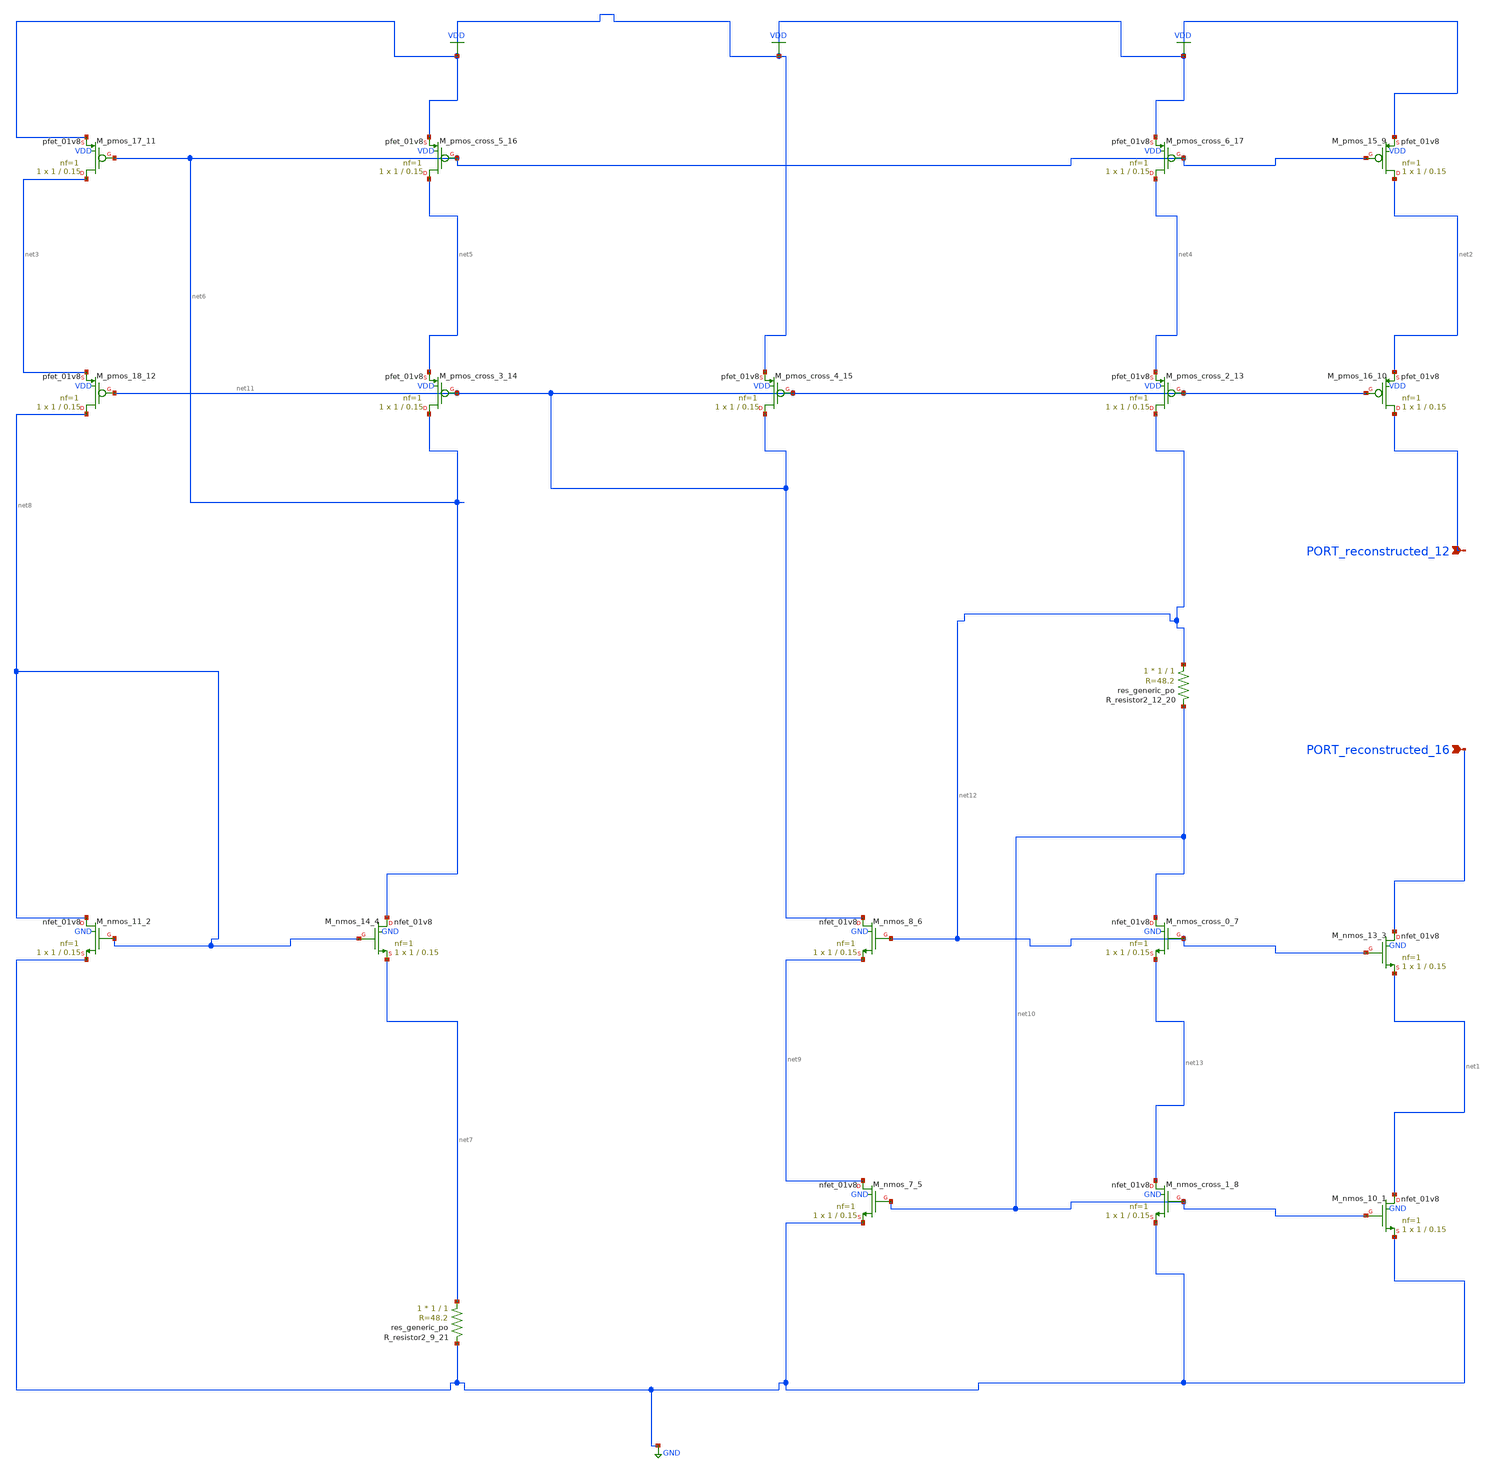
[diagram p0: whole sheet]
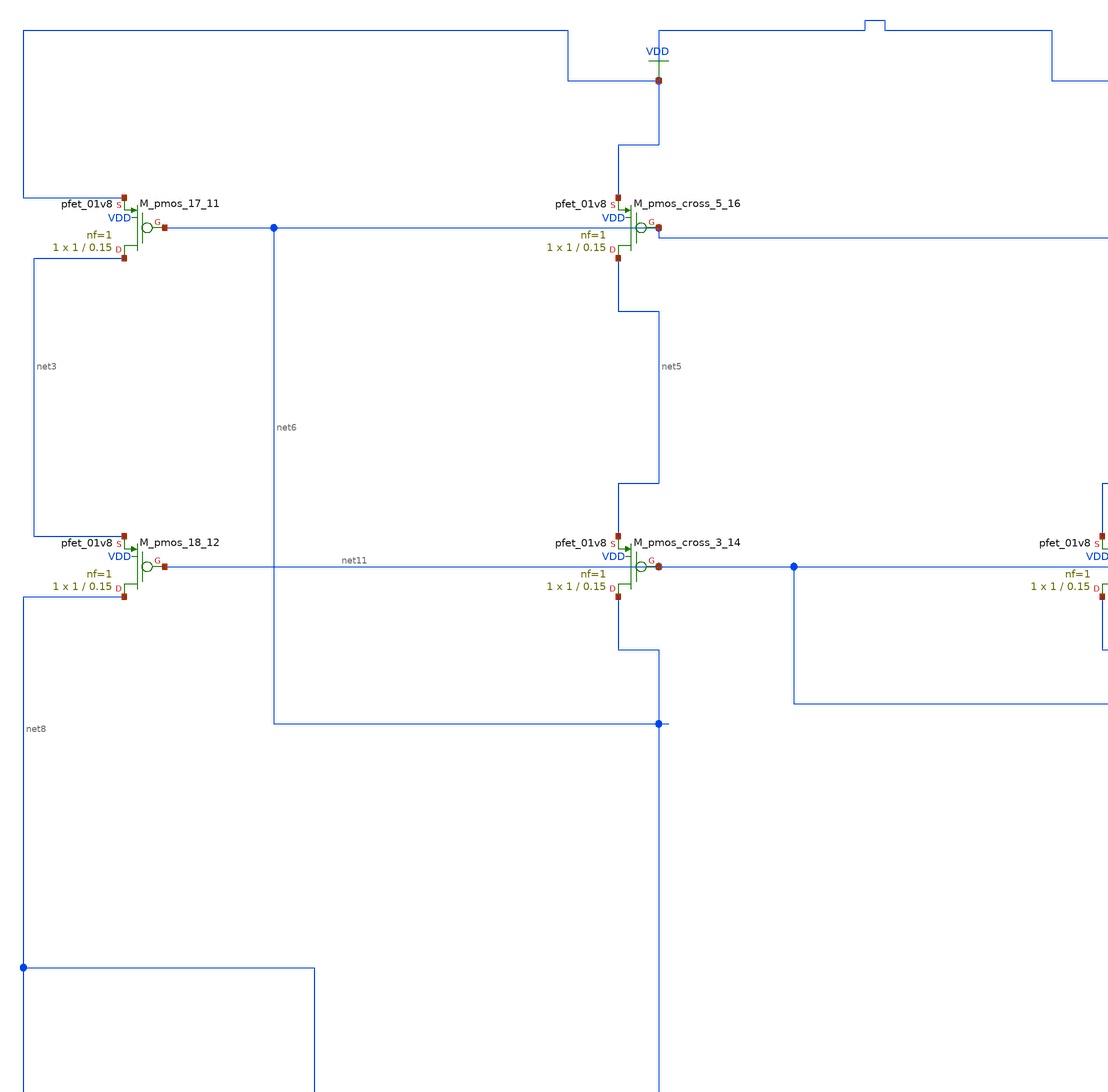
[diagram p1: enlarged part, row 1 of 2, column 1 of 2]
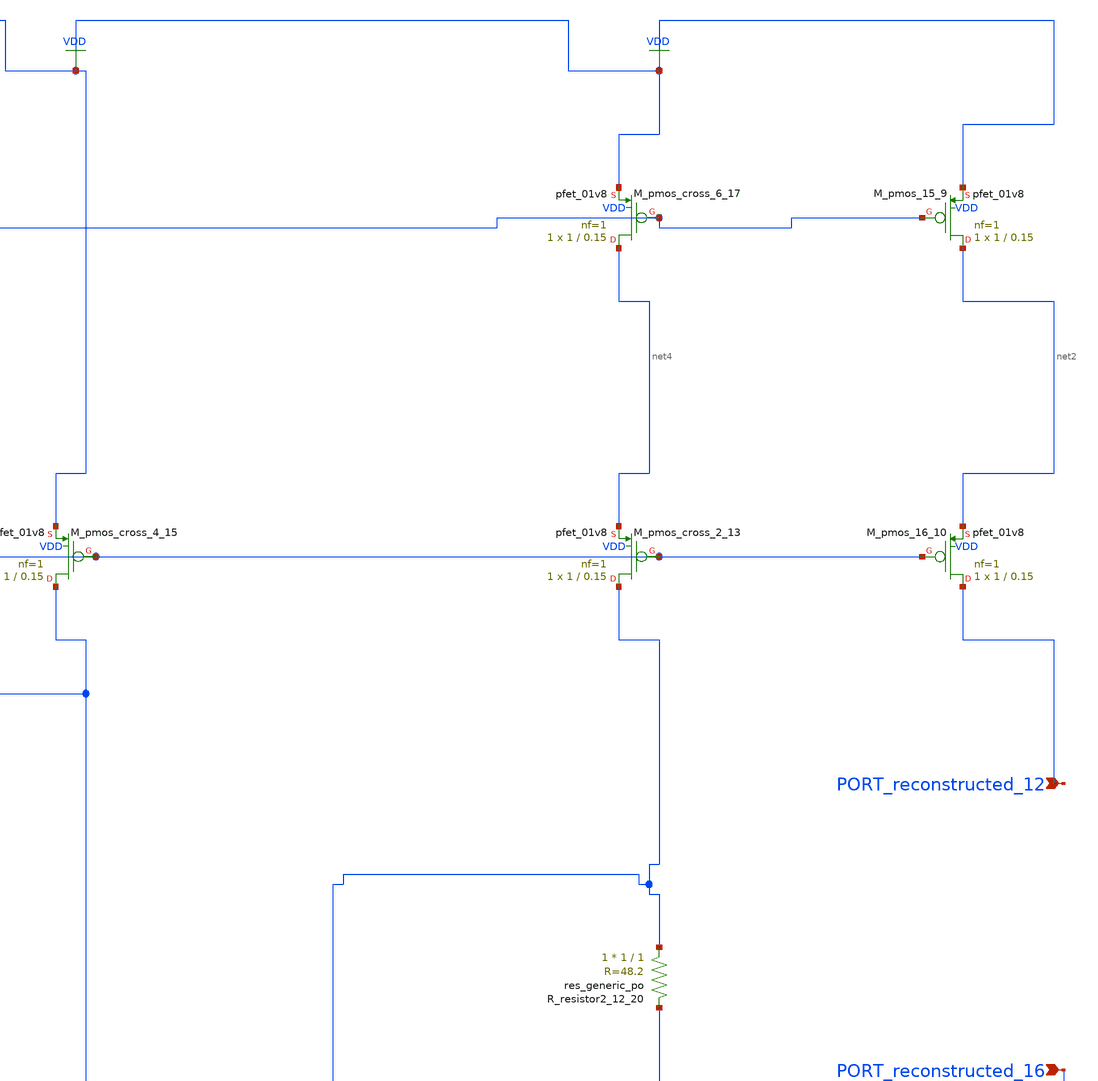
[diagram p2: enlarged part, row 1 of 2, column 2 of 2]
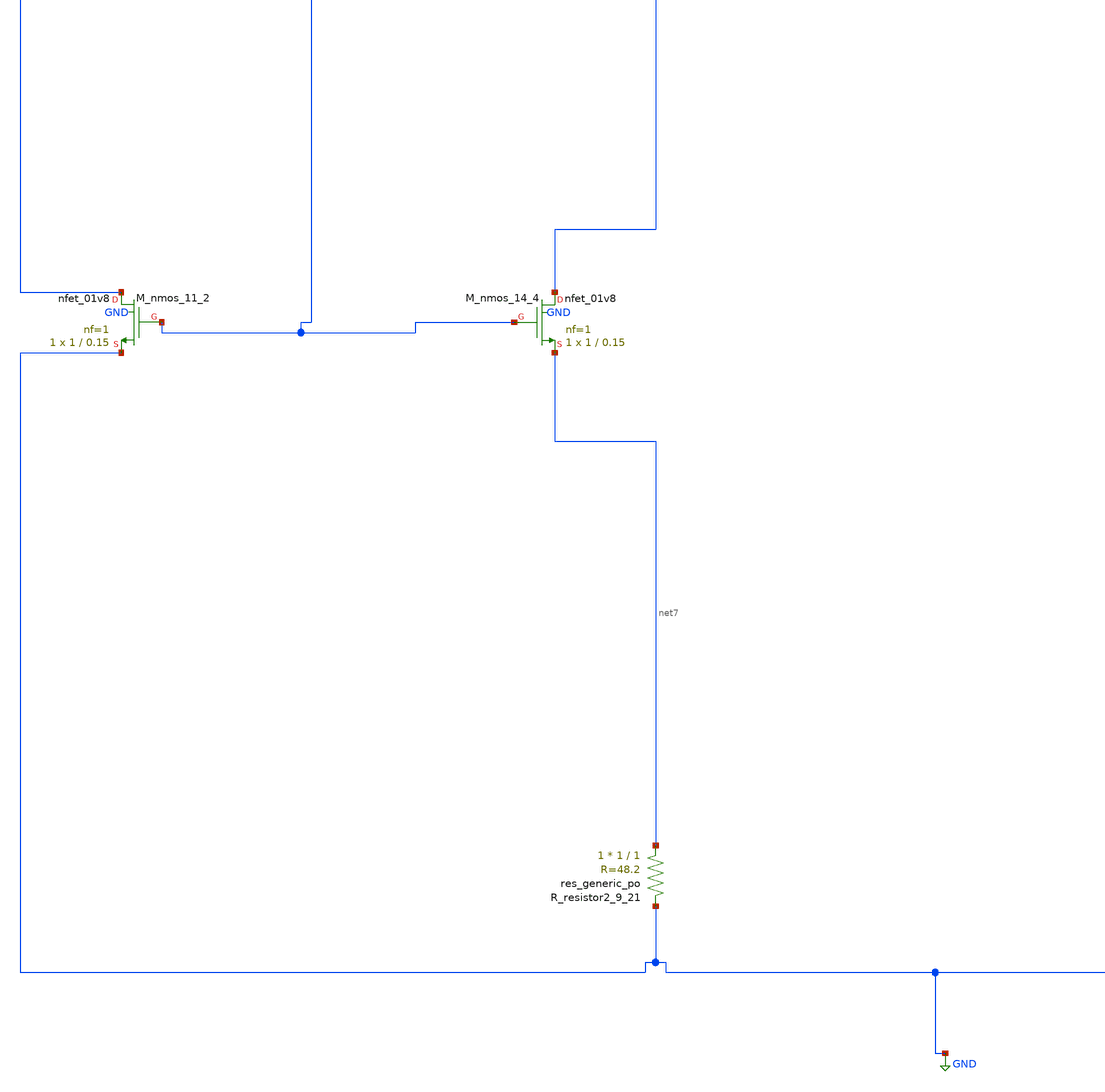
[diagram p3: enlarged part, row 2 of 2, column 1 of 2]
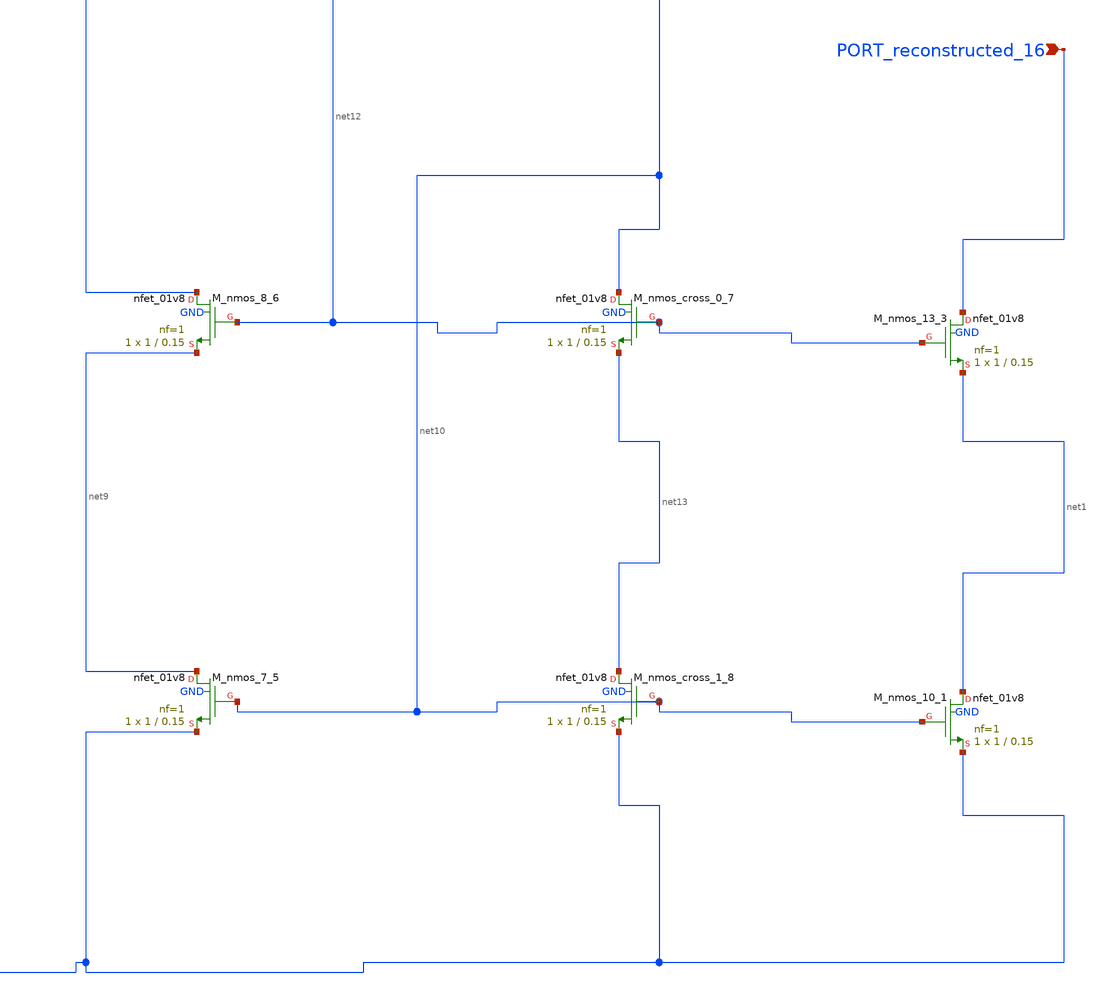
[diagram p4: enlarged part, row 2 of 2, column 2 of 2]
** sch_path: schematics/Image2Net/027.sch
**.subckt 027 PORT_reconstructed_16 PORT_reconstructed_12
*.ipin PORT_reconstructed_16
*.ipin PORT_reconstructed_12
XM_nmos_10_1 net1 net10 GND GND sky130_fd_pr__nfet_01v8 L=0.15 W=1 nf=1 ad='int((1 + 1)/2) * 1 / 1 * 0.29'
+ as='int((1 + 2)/2) * 1 / 1 * 0.29' pd='2*int((1 + 1)/2) * (1 / 1 + 0.29)' ps='2*int((1 + 2)/2) * (1 / 1 + 0.29)'
+ nrd='0.29 / 1 ' nrs='0.29 / 1 ' sa=0 sb=0 sd=0 mult=1 m=1
XM_nmos_11_2 net8 net8 GND GND sky130_fd_pr__nfet_01v8 L=0.15 W=1 nf=1 ad='int((1 + 1)/2) * 1 / 1 * 0.29'
+ as='int((1 + 2)/2) * 1 / 1 * 0.29' pd='2*int((1 + 1)/2) * (1 / 1 + 0.29)' ps='2*int((1 + 2)/2) * (1 / 1 + 0.29)'
+ nrd='0.29 / 1 ' nrs='0.29 / 1 ' sa=0 sb=0 sd=0 mult=1 m=1
XM_nmos_13_3 PORT_reconstructed_16 net12 net1 GND sky130_fd_pr__nfet_01v8 L=0.15 W=1 nf=1 ad='int((1 + 1)/2) * 1 / 1 * 0.29'
+ as='int((1 + 2)/2) * 1 / 1 * 0.29' pd='2*int((1 + 1)/2) * (1 / 1 + 0.29)' ps='2*int((1 + 2)/2) * (1 / 1 + 0.29)'
+ nrd='0.29 / 1 ' nrs='0.29 / 1 ' sa=0 sb=0 sd=0 mult=1 m=1
XM_nmos_14_4 net6 net8 net7 GND sky130_fd_pr__nfet_01v8 L=0.15 W=1 nf=1 ad='int((1 + 1)/2) * 1 / 1 * 0.29'
+ as='int((1 + 2)/2) * 1 / 1 * 0.29' pd='2*int((1 + 1)/2) * (1 / 1 + 0.29)' ps='2*int((1 + 2)/2) * (1 / 1 + 0.29)'
+ nrd='0.29 / 1 ' nrs='0.29 / 1 ' sa=0 sb=0 sd=0 mult=1 m=1
XM_nmos_7_5 net9 net10 GND GND sky130_fd_pr__nfet_01v8 L=0.15 W=1 nf=1 ad='int((1 + 1)/2) * 1 / 1 * 0.29'
+ as='int((1 + 2)/2) * 1 / 1 * 0.29' pd='2*int((1 + 1)/2) * (1 / 1 + 0.29)' ps='2*int((1 + 2)/2) * (1 / 1 + 0.29)'
+ nrd='0.29 / 1 ' nrs='0.29 / 1 ' sa=0 sb=0 sd=0 mult=1 m=1
XM_nmos_8_6 net11 net12 net9 GND sky130_fd_pr__nfet_01v8 L=0.15 W=1 nf=1 ad='int((1 + 1)/2) * 1 / 1 * 0.29'
+ as='int((1 + 2)/2) * 1 / 1 * 0.29' pd='2*int((1 + 1)/2) * (1 / 1 + 0.29)' ps='2*int((1 + 2)/2) * (1 / 1 + 0.29)'
+ nrd='0.29 / 1 ' nrs='0.29 / 1 ' sa=0 sb=0 sd=0 mult=1 m=1
XM_nmos_cross_0_7 net10 net12 net13 GND sky130_fd_pr__nfet_01v8 L=0.15 W=1 nf=1 ad='int((1 + 1)/2) * 1 / 1 * 0.29'
+ as='int((1 + 2)/2) * 1 / 1 * 0.29' pd='2*int((1 + 1)/2) * (1 / 1 + 0.29)' ps='2*int((1 + 2)/2) * (1 / 1 + 0.29)'
+ nrd='0.29 / 1 ' nrs='0.29 / 1 ' sa=0 sb=0 sd=0 mult=1 m=1
XM_nmos_cross_1_8 net13 net10 GND GND sky130_fd_pr__nfet_01v8 L=0.15 W=1 nf=1 ad='int((1 + 1)/2) * 1 / 1 * 0.29'
+ as='int((1 + 2)/2) * 1 / 1 * 0.29' pd='2*int((1 + 1)/2) * (1 / 1 + 0.29)' ps='2*int((1 + 2)/2) * (1 / 1 + 0.29)'
+ nrd='0.29 / 1 ' nrs='0.29 / 1 ' sa=0 sb=0 sd=0 mult=1 m=1
XM_pmos_15_9 net2 net6 VDD VDD sky130_fd_pr__pfet_01v8 L=0.15 W=1 nf=1 ad='int((1 + 1)/2) * 1 / 1 * 0.29'
+ as='int((1 + 2)/2) * 1 / 1 * 0.29' pd='2*int((1 + 1)/2) * (1 / 1 + 0.29)' ps='2*int((1 + 2)/2) * (1 / 1 + 0.29)'
+ nrd='0.29 / 1 ' nrs='0.29 / 1 ' sa=0 sb=0 sd=0 mult=1 m=1
XM_pmos_16_10 PORT_reconstructed_12 net11 net2 VDD sky130_fd_pr__pfet_01v8 L=0.15 W=1 nf=1 ad='int((1 + 1)/2) * 1 / 1 * 0.29'
+ as='int((1 + 2)/2) * 1 / 1 * 0.29' pd='2*int((1 + 1)/2) * (1 / 1 + 0.29)' ps='2*int((1 + 2)/2) * (1 / 1 + 0.29)'
+ nrd='0.29 / 1 ' nrs='0.29 / 1 ' sa=0 sb=0 sd=0 mult=1 m=1
XM_pmos_17_11 net3 net6 VDD VDD sky130_fd_pr__pfet_01v8 L=0.15 W=1 nf=1 ad='int((1 + 1)/2) * 1 / 1 * 0.29'
+ as='int((1 + 2)/2) * 1 / 1 * 0.29' pd='2*int((1 + 1)/2) * (1 / 1 + 0.29)' ps='2*int((1 + 2)/2) * (1 / 1 + 0.29)'
+ nrd='0.29 / 1 ' nrs='0.29 / 1 ' sa=0 sb=0 sd=0 mult=1 m=1
XM_pmos_18_12 net8 net11 net3 VDD sky130_fd_pr__pfet_01v8 L=0.15 W=1 nf=1 ad='int((1 + 1)/2) * 1 / 1 * 0.29'
+ as='int((1 + 2)/2) * 1 / 1 * 0.29' pd='2*int((1 + 1)/2) * (1 / 1 + 0.29)' ps='2*int((1 + 2)/2) * (1 / 1 + 0.29)'
+ nrd='0.29 / 1 ' nrs='0.29 / 1 ' sa=0 sb=0 sd=0 mult=1 m=1
XM_pmos_cross_2_13 net12 net11 net4 VDD sky130_fd_pr__pfet_01v8 L=0.15 W=1 nf=1 ad='int((1 + 1)/2) * 1 / 1 * 0.29'
+ as='int((1 + 2)/2) * 1 / 1 * 0.29' pd='2*int((1 + 1)/2) * (1 / 1 + 0.29)' ps='2*int((1 + 2)/2) * (1 / 1 + 0.29)'
+ nrd='0.29 / 1 ' nrs='0.29 / 1 ' sa=0 sb=0 sd=0 mult=1 m=1
XM_pmos_cross_3_14 net6 net11 net5 VDD sky130_fd_pr__pfet_01v8 L=0.15 W=1 nf=1 ad='int((1 + 1)/2) * 1 / 1 * 0.29'
+ as='int((1 + 2)/2) * 1 / 1 * 0.29' pd='2*int((1 + 1)/2) * (1 / 1 + 0.29)' ps='2*int((1 + 2)/2) * (1 / 1 + 0.29)'
+ nrd='0.29 / 1 ' nrs='0.29 / 1 ' sa=0 sb=0 sd=0 mult=1 m=1
XM_pmos_cross_4_15 net11 net11 VDD VDD sky130_fd_pr__pfet_01v8 L=0.15 W=1 nf=1 ad='int((1 + 1)/2) * 1 / 1 * 0.29'
+ as='int((1 + 2)/2) * 1 / 1 * 0.29' pd='2*int((1 + 1)/2) * (1 / 1 + 0.29)' ps='2*int((1 + 2)/2) * (1 / 1 + 0.29)'
+ nrd='0.29 / 1 ' nrs='0.29 / 1 ' sa=0 sb=0 sd=0 mult=1 m=1
XM_pmos_cross_5_16 net5 net6 VDD VDD sky130_fd_pr__pfet_01v8 L=0.15 W=1 nf=1 ad='int((1 + 1)/2) * 1 / 1 * 0.29'
+ as='int((1 + 2)/2) * 1 / 1 * 0.29' pd='2*int((1 + 1)/2) * (1 / 1 + 0.29)' ps='2*int((1 + 2)/2) * (1 / 1 + 0.29)'
+ nrd='0.29 / 1 ' nrs='0.29 / 1 ' sa=0 sb=0 sd=0 mult=1 m=1
XM_pmos_cross_6_17 net4 net6 VDD VDD sky130_fd_pr__pfet_01v8 L=0.15 W=1 nf=1 ad='int((1 + 1)/2) * 1 / 1 * 0.29'
+ as='int((1 + 2)/2) * 1 / 1 * 0.29' pd='2*int((1 + 1)/2) * (1 / 1 + 0.29)' ps='2*int((1 + 2)/2) * (1 / 1 + 0.29)'
+ nrd='0.29 / 1 ' nrs='0.29 / 1 ' sa=0 sb=0 sd=0 mult=1 m=1
XR_resistor2_12_20 net12 net10 sky130_fd_pr__res_generic_po W=1 L=1 m=1
XR_resistor2_9_21 net7 GND sky130_fd_pr__res_generic_po W=1 L=1 m=1
**.ends
.GLOBAL GND
.GLOBAL VDD
.end
